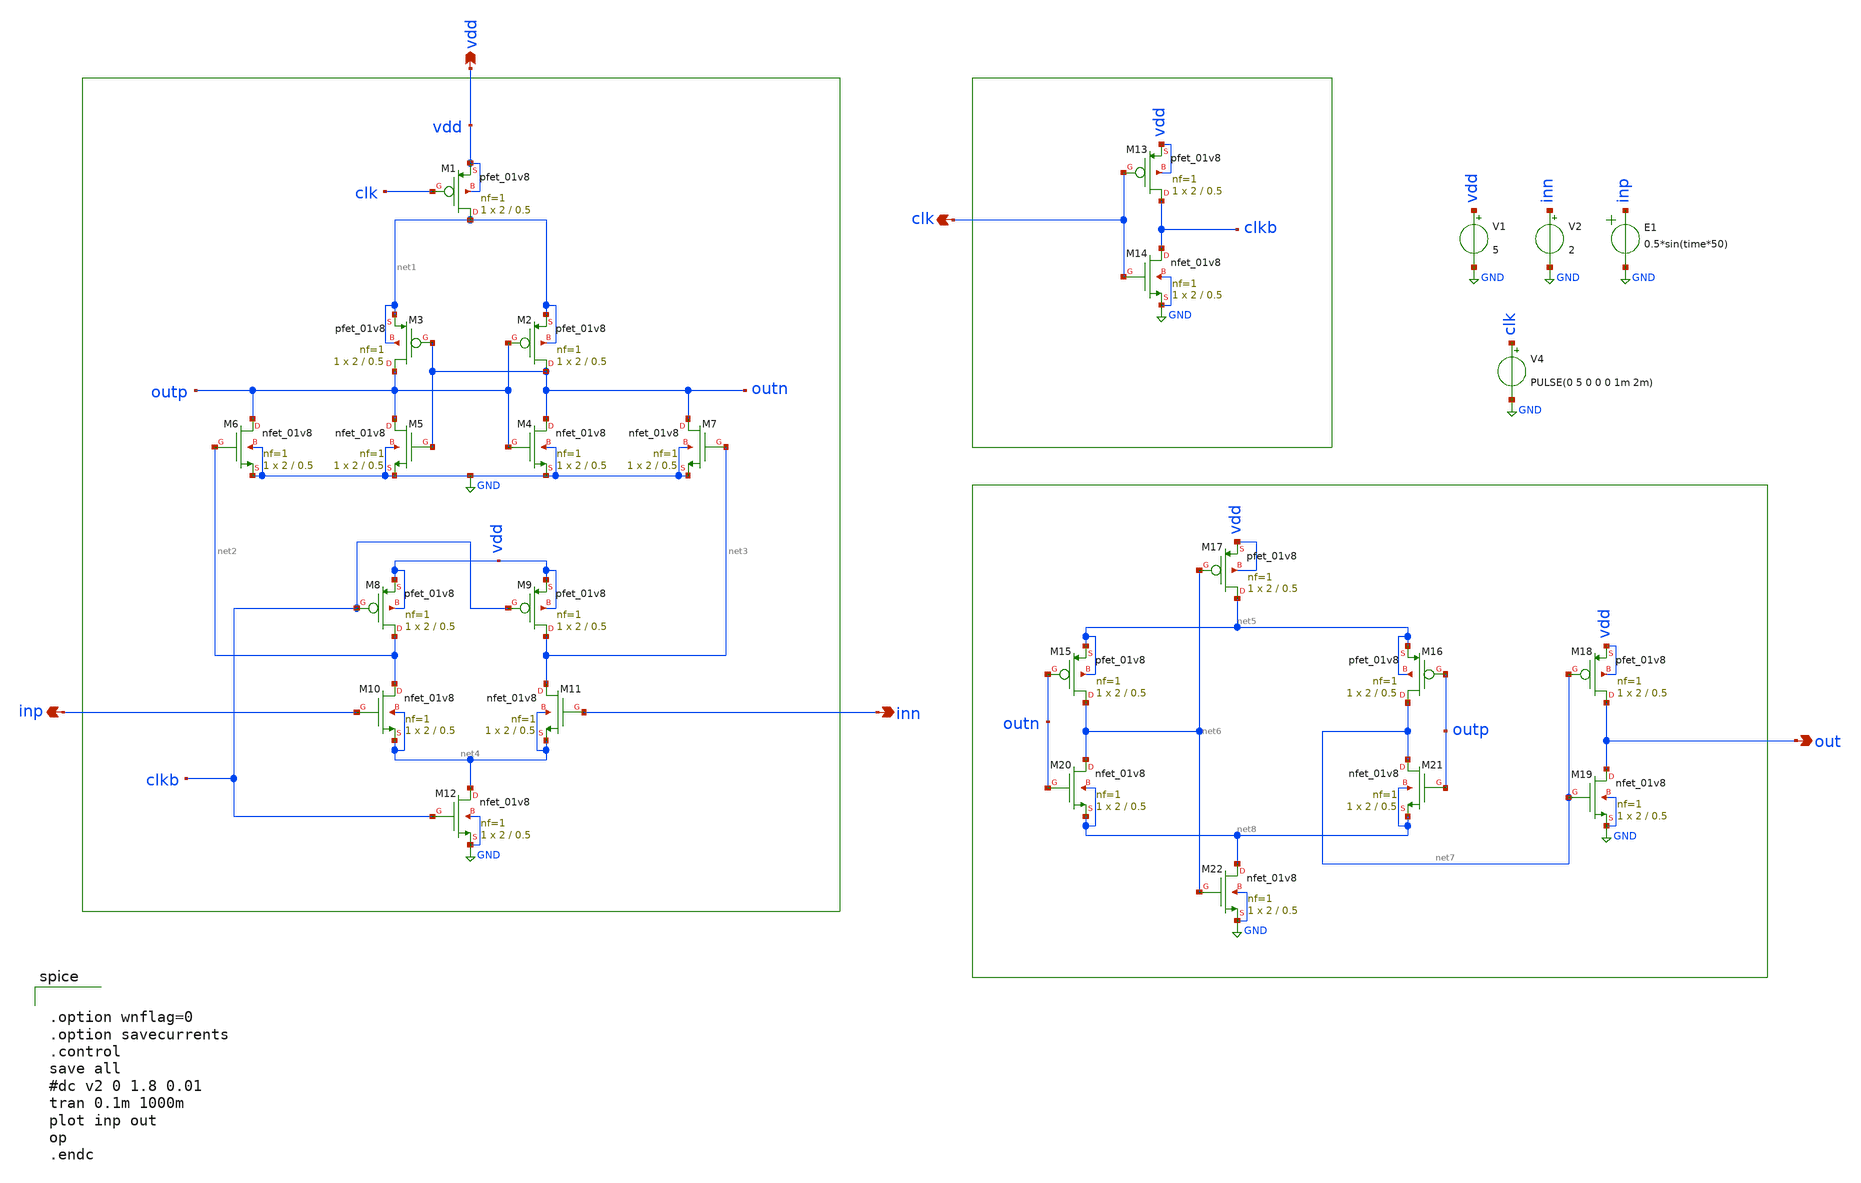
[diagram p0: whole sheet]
** sch_path: FP_Mixed_Signal.sch
**.subckt FP_Mixed_Signal inp inn clk vdd out
*.opin inp
*.opin inn
*.opin clk
*.opin vdd
*.opin out
XM1 net1 clk vdd vdd sky130_fd_pr__pfet_01v8 L=0.5 W=2 nf=1 ad='int((nf+1)/2) * W/nf * 0.29' as='int((nf+2)/2) * W/nf * 0.29'
+ pd='2*int((nf+1)/2) * (W/nf + 0.29)' ps='2*int((nf+2)/2) * (W/nf + 0.29)' nrd='0.29 / W' nrs='0.29 / W'
+ sa=0 sb=0 sd=0 mult=1 m=1
XM2 outn outp net1 net1 sky130_fd_pr__pfet_01v8 L=0.5 W=2 nf=1 ad='int((nf+1)/2) * W/nf * 0.29' as='int((nf+2)/2) * W/nf * 0.29'
+ pd='2*int((nf+1)/2) * (W/nf + 0.29)' ps='2*int((nf+2)/2) * (W/nf + 0.29)' nrd='0.29 / W' nrs='0.29 / W'
+ sa=0 sb=0 sd=0 mult=1 m=1
XM3 outp outn net1 net1 sky130_fd_pr__pfet_01v8 L=0.5 W=2 nf=1 ad='int((nf+1)/2) * W/nf * 0.29' as='int((nf+2)/2) * W/nf * 0.29'
+ pd='2*int((nf+1)/2) * (W/nf + 0.29)' ps='2*int((nf+2)/2) * (W/nf + 0.29)' nrd='0.29 / W' nrs='0.29 / W'
+ sa=0 sb=0 sd=0 mult=1 m=1
XM4 outn outp GND GND sky130_fd_pr__nfet_01v8 L=0.5 W=2 nf=1 ad='int((nf+1)/2) * W/nf * 0.29' as='int((nf+2)/2) * W/nf * 0.29'
+ pd='2*int((nf+1)/2) * (W/nf + 0.29)' ps='2*int((nf+2)/2) * (W/nf + 0.29)' nrd='0.29 / W' nrs='0.29 / W'
+ sa=0 sb=0 sd=0 mult=1 m=1
XM5 outp outn GND GND sky130_fd_pr__nfet_01v8 L=0.5 W=2 nf=1 ad='int((nf+1)/2) * W/nf * 0.29' as='int((nf+2)/2) * W/nf * 0.29'
+ pd='2*int((nf+1)/2) * (W/nf + 0.29)' ps='2*int((nf+2)/2) * (W/nf + 0.29)' nrd='0.29 / W' nrs='0.29 / W'
+ sa=0 sb=0 sd=0 mult=1 m=1
XM6 outp net2 GND GND sky130_fd_pr__nfet_01v8 L=0.5 W=2 nf=1 ad='int((nf+1)/2) * W/nf * 0.29' as='int((nf+2)/2) * W/nf * 0.29'
+ pd='2*int((nf+1)/2) * (W/nf + 0.29)' ps='2*int((nf+2)/2) * (W/nf + 0.29)' nrd='0.29 / W' nrs='0.29 / W'
+ sa=0 sb=0 sd=0 mult=1 m=1
XM7 outn net3 GND GND sky130_fd_pr__nfet_01v8 L=0.5 W=2 nf=1 ad='int((nf+1)/2) * W/nf * 0.29' as='int((nf+2)/2) * W/nf * 0.29'
+ pd='2*int((nf+1)/2) * (W/nf + 0.29)' ps='2*int((nf+2)/2) * (W/nf + 0.29)' nrd='0.29 / W' nrs='0.29 / W'
+ sa=0 sb=0 sd=0 mult=1 m=1
XM8 net2 clkb vdd vdd sky130_fd_pr__pfet_01v8 L=0.5 W=2 nf=1 ad='int((nf+1)/2) * W/nf * 0.29' as='int((nf+2)/2) * W/nf * 0.29'
+ pd='2*int((nf+1)/2) * (W/nf + 0.29)' ps='2*int((nf+2)/2) * (W/nf + 0.29)' nrd='0.29 / W' nrs='0.29 / W'
+ sa=0 sb=0 sd=0 mult=1 m=1
XM9 net3 clkb vdd vdd sky130_fd_pr__pfet_01v8 L=0.5 W=2 nf=1 ad='int((nf+1)/2) * W/nf * 0.29' as='int((nf+2)/2) * W/nf * 0.29'
+ pd='2*int((nf+1)/2) * (W/nf + 0.29)' ps='2*int((nf+2)/2) * (W/nf + 0.29)' nrd='0.29 / W' nrs='0.29 / W'
+ sa=0 sb=0 sd=0 mult=1 m=1
XM10 net2 inp net4 net4 sky130_fd_pr__nfet_01v8 L=0.5 W=2 nf=1 ad='int((nf+1)/2) * W/nf * 0.29' as='int((nf+2)/2) * W/nf * 0.29'
+ pd='2*int((nf+1)/2) * (W/nf + 0.29)' ps='2*int((nf+2)/2) * (W/nf + 0.29)' nrd='0.29 / W' nrs='0.29 / W'
+ sa=0 sb=0 sd=0 mult=1 m=1
XM11 net3 inn net4 net4 sky130_fd_pr__nfet_01v8 L=0.5 W=2 nf=1 ad='int((nf+1)/2) * W/nf * 0.29' as='int((nf+2)/2) * W/nf * 0.29'
+ pd='2*int((nf+1)/2) * (W/nf + 0.29)' ps='2*int((nf+2)/2) * (W/nf + 0.29)' nrd='0.29 / W' nrs='0.29 / W'
+ sa=0 sb=0 sd=0 mult=1 m=1
XM12 net4 clkb GND GND sky130_fd_pr__nfet_01v8 L=0.5 W=2 nf=1 ad='int((nf+1)/2) * W/nf * 0.29' as='int((nf+2)/2) * W/nf * 0.29'
+ pd='2*int((nf+1)/2) * (W/nf + 0.29)' ps='2*int((nf+2)/2) * (W/nf + 0.29)' nrd='0.29 / W' nrs='0.29 / W'
+ sa=0 sb=0 sd=0 mult=1 m=1
XM13 clkb clk vdd vdd sky130_fd_pr__pfet_01v8 L=0.5 W=2 nf=1 ad='int((nf+1)/2) * W/nf * 0.29' as='int((nf+2)/2) * W/nf * 0.29'
+ pd='2*int((nf+1)/2) * (W/nf + 0.29)' ps='2*int((nf+2)/2) * (W/nf + 0.29)' nrd='0.29 / W' nrs='0.29 / W'
+ sa=0 sb=0 sd=0 mult=1 m=1
XM14 clkb clk GND GND sky130_fd_pr__nfet_01v8 L=0.5 W=2 nf=1 ad='int((nf+1)/2) * W/nf * 0.29' as='int((nf+2)/2) * W/nf * 0.29'
+ pd='2*int((nf+1)/2) * (W/nf + 0.29)' ps='2*int((nf+2)/2) * (W/nf + 0.29)' nrd='0.29 / W' nrs='0.29 / W'
+ sa=0 sb=0 sd=0 mult=1 m=1
XM15 net6 outn net5 net5 sky130_fd_pr__pfet_01v8 L=0.5 W=2 nf=1 ad='int((nf+1)/2) * W/nf * 0.29' as='int((nf+2)/2) * W/nf * 0.29'
+ pd='2*int((nf+1)/2) * (W/nf + 0.29)' ps='2*int((nf+2)/2) * (W/nf + 0.29)' nrd='0.29 / W' nrs='0.29 / W'
+ sa=0 sb=0 sd=0 mult=1 m=1
XM16 net7 outp net5 net5 sky130_fd_pr__pfet_01v8 L=0.5 W=2 nf=1 ad='int((nf+1)/2) * W/nf * 0.29' as='int((nf+2)/2) * W/nf * 0.29'
+ pd='2*int((nf+1)/2) * (W/nf + 0.29)' ps='2*int((nf+2)/2) * (W/nf + 0.29)' nrd='0.29 / W' nrs='0.29 / W'
+ sa=0 sb=0 sd=0 mult=1 m=1
XM17 net5 net6 vdd vdd sky130_fd_pr__pfet_01v8 L=0.5 W=2 nf=1 ad='int((nf+1)/2) * W/nf * 0.29' as='int((nf+2)/2) * W/nf * 0.29'
+ pd='2*int((nf+1)/2) * (W/nf + 0.29)' ps='2*int((nf+2)/2) * (W/nf + 0.29)' nrd='0.29 / W' nrs='0.29 / W'
+ sa=0 sb=0 sd=0 mult=1 m=1
XM18 out net7 vdd vdd sky130_fd_pr__pfet_01v8 L=0.5 W=2 nf=1 ad='int((nf+1)/2) * W/nf * 0.29' as='int((nf+2)/2) * W/nf * 0.29'
+ pd='2*int((nf+1)/2) * (W/nf + 0.29)' ps='2*int((nf+2)/2) * (W/nf + 0.29)' nrd='0.29 / W' nrs='0.29 / W'
+ sa=0 sb=0 sd=0 mult=1 m=1
XM19 out net7 GND GND sky130_fd_pr__nfet_01v8 L=0.5 W=2 nf=1 ad='int((nf+1)/2) * W/nf * 0.29' as='int((nf+2)/2) * W/nf * 0.29'
+ pd='2*int((nf+1)/2) * (W/nf + 0.29)' ps='2*int((nf+2)/2) * (W/nf + 0.29)' nrd='0.29 / W' nrs='0.29 / W'
+ sa=0 sb=0 sd=0 mult=1 m=1
XM20 net6 outn net8 net8 sky130_fd_pr__nfet_01v8 L=0.5 W=2 nf=1 ad='int((nf+1)/2) * W/nf * 0.29' as='int((nf+2)/2) * W/nf * 0.29'
+ pd='2*int((nf+1)/2) * (W/nf + 0.29)' ps='2*int((nf+2)/2) * (W/nf + 0.29)' nrd='0.29 / W' nrs='0.29 / W'
+ sa=0 sb=0 sd=0 mult=1 m=1
XM21 net7 outp net8 net8 sky130_fd_pr__nfet_01v8 L=0.5 W=2 nf=1 ad='int((nf+1)/2) * W/nf * 0.29' as='int((nf+2)/2) * W/nf * 0.29'
+ pd='2*int((nf+1)/2) * (W/nf + 0.29)' ps='2*int((nf+2)/2) * (W/nf + 0.29)' nrd='0.29 / W' nrs='0.29 / W'
+ sa=0 sb=0 sd=0 mult=1 m=1
XM22 net8 net6 GND GND sky130_fd_pr__nfet_01v8 L=0.5 W=2 nf=1 ad='int((nf+1)/2) * W/nf * 0.29' as='int((nf+2)/2) * W/nf * 0.29'
+ pd='2*int((nf+1)/2) * (W/nf + 0.29)' ps='2*int((nf+2)/2) * (W/nf + 0.29)' nrd='0.29 / W' nrs='0.29 / W'
+ sa=0 sb=0 sd=0 mult=1 m=1
V1 vdd GND 5
V2 inn GND 2
V4 clk GND PULSE(0 5 0 0 0 1m 2m)
E1 inp GND VOL=' 0.5*sin(time*50) '
**** begin user architecture code
 .lib $::SKYWATER_MODELS/models/sky130.lib.spice tt
.param mc_mm_switch=0
.param mc_pr_switch=1



.option wnflag=0
.option savecurrents
.control
save all
#dc v2 0 1.8 0.01
tran 0.1m 1000m
plot inp out
op
.endc


**** end user architecture code
**.ends
.GLOBAL GND
.end
